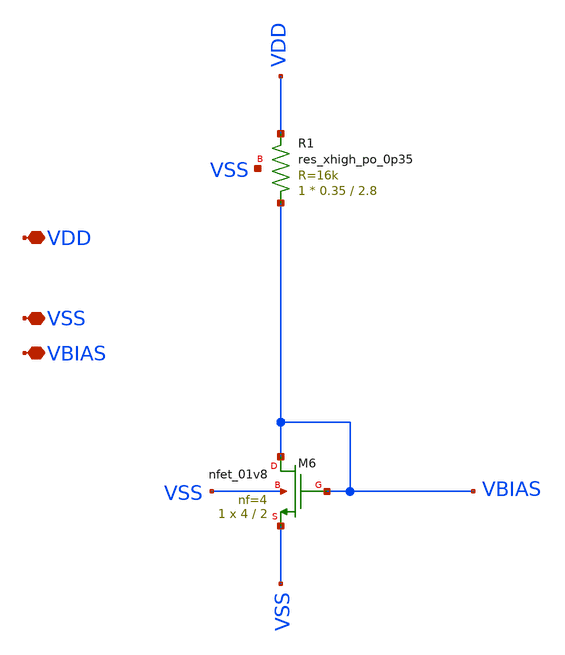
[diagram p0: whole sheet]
** sch_path: xschem/vbias_resistor.sch
**.subckt vbias_resistor VDD VSS VBIAS
*.iopin VDD
*.iopin VSS
*.iopin VBIAS
XM6 VBIAS VBIAS VSS VSS sky130_fd_pr__nfet_01v8 L=2 W=4 nf=4 ad='int((nf+1)/2) * W/nf * 0.29' as='int((nf+2)/2) * W/nf * 0.29'
+ pd='2*int((nf+1)/2) * (W/nf + 0.29)' ps='2*int((nf+2)/2) * (W/nf + 0.29)' nrd='0.29 / W' nrs='0.29 / W'
+ sa=0 sb=0 sd=0 mult=1 m=1
XR1 VBIAS VDD VSS sky130_fd_pr__res_xhigh_po_0p35 L=2.8 mult=1 m=1
**.ends
.end
